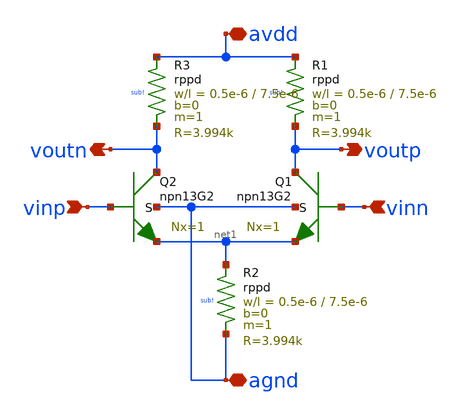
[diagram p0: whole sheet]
** sch_path: xschem/comparator.sch
**.subckt comparator avdd vinp voutp agnd vinn voutn
*.iopin avdd
*.ipin vinp
*.opin voutp
*.iopin agnd
*.ipin vinn
*.opin voutn
XR2 net1 agnd sub! rppd w=0.5e-6 l=7.5e-6 m=1 b=0 mm_ok=1
XQ1 voutp vinn net1 agnd npn13G2 Nx=1 mm_ok=1
XQ2 voutn vinp net1 agnd npn13G2 Nx=1 mm_ok=1
XR1 avdd voutp sub! rppd w=0.5e-6 l=7.5e-6 m=1 b=0 mm_ok=1
XR3 avdd voutn sub! rppd w=0.5e-6 l=7.5e-6 m=1 b=0 mm_ok=1
**.ends
.end
